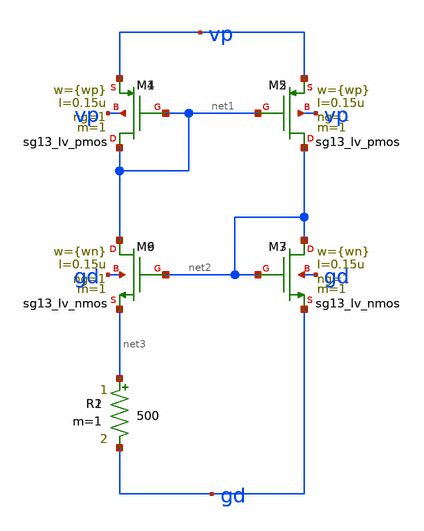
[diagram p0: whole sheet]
** sch_path: charge_pump/curr_source.sch
**.subckt curr_source
XM1 net1 net1 vp vp sg13_lv_pmos w={wp} l=0.15u ng=1 m=1 mm_ok=1
XM2 net2 net1 vp vp sg13_lv_pmos w={wp} l=0.15u ng=1 m=1 mm_ok=1
XM9 net1 net2 net3 gd sg13_lv_nmos w={wn} l=0.15u ng=1 m=1 mm_ok=1
XM3 net2 net2 gd gd sg13_lv_nmos w={wn} l=0.15u ng=1 m=1 mm_ok=1
R1 net3 gd 500 m=1
XM4 net1 net1 vp vp sg13_lv_pmos w={wp} l=0.15u ng=1 m=1 mm_ok=1
XM5 net2 net1 vp vp sg13_lv_pmos w={wp} l=0.15u ng=1 m=1 mm_ok=1
XM6 net1 net2 net3 gd sg13_lv_nmos w={wn} l=0.15u ng=1 m=1 mm_ok=1
XM7 net2 net2 gd gd sg13_lv_nmos w={wn} l=0.15u ng=1 m=1 mm_ok=1
R2 net3 gd 500 m=1
**.ends
.end
